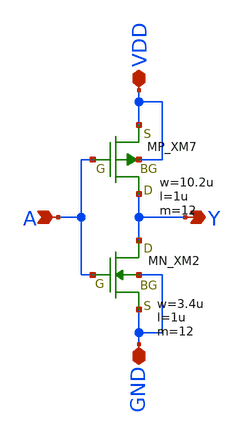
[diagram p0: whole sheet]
** sch_path: openIP62_rev1.0/IP62/Technology/tech/symbols/Xschem/IP62_5_stdcell/INV_X12.sch
**.subckt INV_X12 A Y GND VDD
*.ipin A
*.opin Y
*.iopin GND
*.iopin VDD
XM7 Y A VDD VDD PMOS w=10.2u l=1u as=0 ad=0 ps=0 pd=0 nrd=0 nrs=0 m=12
XM2 Y A GND GND NMOS w=3.4u l=1u as=0 ad=0 ps=0 pd=0 nrd=0 nrs=0 m=12
**.ends
.end
